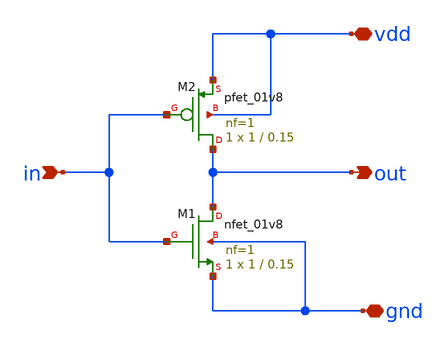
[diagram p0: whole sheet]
** sch_path: inverter/inverter_baru.sch
**.subckt inverter_baru in vdd out gnd
*.ipin in
*.iopin vdd
*.opin out
*.iopin gnd
XM1 out in gnd gnd sky130_fd_pr__nfet_01v8 L=0.15 W=1 nf=1 ad='int((nf+1)/2) * W/nf * 0.29' as='int((nf+2)/2) * W/nf * 0.29'
+ pd='2*int((nf+1)/2) * (W/nf + 0.29)' ps='2*int((nf+2)/2) * (W/nf + 0.29)' nrd='0.29 / W' nrs='0.29 / W'
+ sa=0 sb=0 sd=0 mult=1 m=1
XM2 out in vdd vdd sky130_fd_pr__pfet_01v8 L=0.15 W=1 nf=1 ad='int((nf+1)/2) * W/nf * 0.29' as='int((nf+2)/2) * W/nf * 0.29'
+ pd='2*int((nf+1)/2) * (W/nf + 0.29)' ps='2*int((nf+2)/2) * (W/nf + 0.29)' nrd='0.29 / W' nrs='0.29 / W'
+ sa=0 sb=0 sd=0 mult=1 m=1
**.ends
.end
